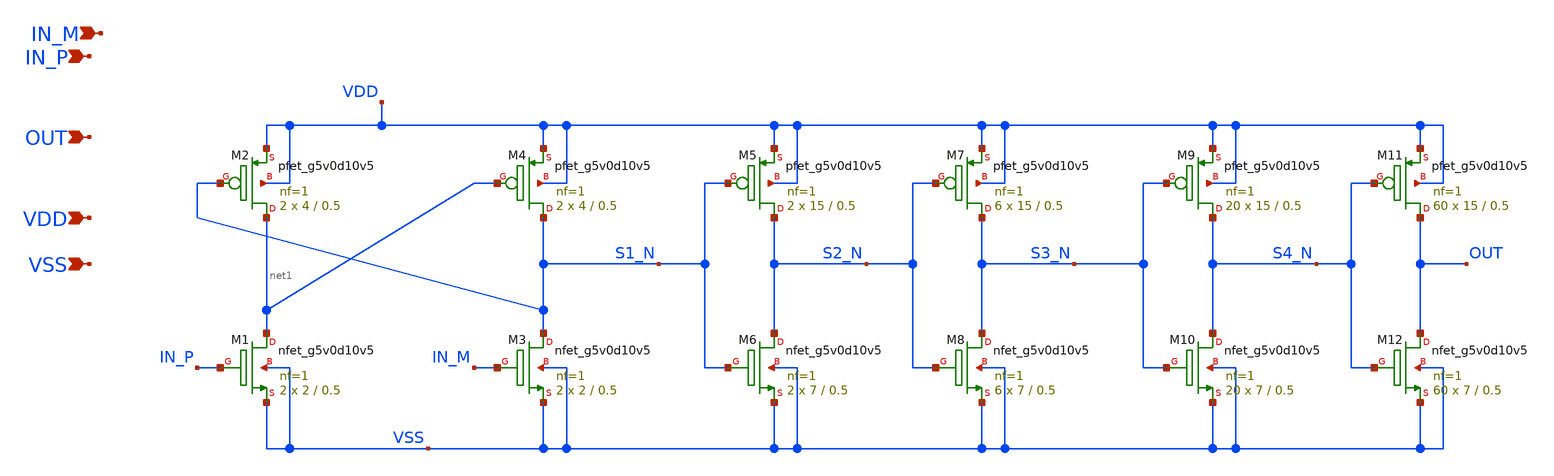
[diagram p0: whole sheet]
** sch_path: images/iic-osic-tools/addons/examples/open-pmic/design/power-stage/gate_drive.sch
**.subckt gate_drive IN_M IN_P OUT VDD VSS
*.ipin IN_M
*.ipin IN_P
*.ipin OUT
*.ipin VDD
*.ipin VSS
XM1 net1 IN_P VSS VSS sky130_fd_pr__nfet_g5v0d10v5 L=0.5 W=2 nf=1 ad='int((nf+1)/2) * W/nf * 0.29' as='int((nf+2)/2) * W/nf * 0.29'
+ pd='2*int((nf+1)/2) * (W/nf + 0.29)' ps='2*int((nf+2)/2) * (W/nf + 0.29)' nrd='0.29 / W' nrs='0.29 / W'
+ sa=0 sb=0 sd=0 mult=2 m=2
XM2 net1 S1_N VDD VDD sky130_fd_pr__pfet_g5v0d10v5 L=0.5 W=4 nf=1 ad='int((nf+1)/2) * W/nf * 0.29' as='int((nf+2)/2) * W/nf * 0.29'
+ pd='2*int((nf+1)/2) * (W/nf + 0.29)' ps='2*int((nf+2)/2) * (W/nf + 0.29)' nrd='0.29 / W' nrs='0.29 / W'
+ sa=0 sb=0 sd=0 mult=2 m=2
XM3 S1_N IN_M VSS VSS sky130_fd_pr__nfet_g5v0d10v5 L=0.5 W=2 nf=1 ad='int((nf+1)/2) * W/nf * 0.29' as='int((nf+2)/2) * W/nf * 0.29'
+ pd='2*int((nf+1)/2) * (W/nf + 0.29)' ps='2*int((nf+2)/2) * (W/nf + 0.29)' nrd='0.29 / W' nrs='0.29 / W'
+ sa=0 sb=0 sd=0 mult=2 m=2
XM4 S1_N net1 VDD VDD sky130_fd_pr__pfet_g5v0d10v5 L=0.5 W=4 nf=1 ad='int((nf+1)/2) * W/nf * 0.29' as='int((nf+2)/2) * W/nf * 0.29'
+ pd='2*int((nf+1)/2) * (W/nf + 0.29)' ps='2*int((nf+2)/2) * (W/nf + 0.29)' nrd='0.29 / W' nrs='0.29 / W'
+ sa=0 sb=0 sd=0 mult=2 m=2
XM5 S2_N S1_N VDD VDD sky130_fd_pr__pfet_g5v0d10v5 L=0.5 W=15 nf=1 ad='int((nf+1)/2) * W/nf * 0.29' as='int((nf+2)/2) * W/nf * 0.29'
+ pd='2*int((nf+1)/2) * (W/nf + 0.29)' ps='2*int((nf+2)/2) * (W/nf + 0.29)' nrd='0.29 / W' nrs='0.29 / W'
+ sa=0 sb=0 sd=0 mult=2 m=2
XM6 S2_N S1_N VSS VSS sky130_fd_pr__nfet_g5v0d10v5 L=0.5 W=7 nf=1 ad='int((nf+1)/2) * W/nf * 0.29' as='int((nf+2)/2) * W/nf * 0.29'
+ pd='2*int((nf+1)/2) * (W/nf + 0.29)' ps='2*int((nf+2)/2) * (W/nf + 0.29)' nrd='0.29 / W' nrs='0.29 / W'
+ sa=0 sb=0 sd=0 mult=2 m=2
XM7 S3_N S2_N VDD VDD sky130_fd_pr__pfet_g5v0d10v5 L=0.5 W=15 nf=1 ad='int((nf+1)/2) * W/nf * 0.29' as='int((nf+2)/2) * W/nf * 0.29'
+ pd='2*int((nf+1)/2) * (W/nf + 0.29)' ps='2*int((nf+2)/2) * (W/nf + 0.29)' nrd='0.29 / W' nrs='0.29 / W'
+ sa=0 sb=0 sd=0 mult=6 m=6
XM8 S3_N S2_N VSS VSS sky130_fd_pr__nfet_g5v0d10v5 L=0.5 W=7 nf=1 ad='int((nf+1)/2) * W/nf * 0.29' as='int((nf+2)/2) * W/nf * 0.29'
+ pd='2*int((nf+1)/2) * (W/nf + 0.29)' ps='2*int((nf+2)/2) * (W/nf + 0.29)' nrd='0.29 / W' nrs='0.29 / W'
+ sa=0 sb=0 sd=0 mult=6 m=6
XM9 S4_N S3_N VDD VDD sky130_fd_pr__pfet_g5v0d10v5 L=0.5 W=15 nf=1 ad='int((nf+1)/2) * W/nf * 0.29' as='int((nf+2)/2) * W/nf * 0.29'
+ pd='2*int((nf+1)/2) * (W/nf + 0.29)' ps='2*int((nf+2)/2) * (W/nf + 0.29)' nrd='0.29 / W' nrs='0.29 / W'
+ sa=0 sb=0 sd=0 mult=20 m=20
XM10 S4_N S3_N VSS VSS sky130_fd_pr__nfet_g5v0d10v5 L=0.5 W=7 nf=1 ad='int((nf+1)/2) * W/nf * 0.29' as='int((nf+2)/2) * W/nf * 0.29'
+ pd='2*int((nf+1)/2) * (W/nf + 0.29)' ps='2*int((nf+2)/2) * (W/nf + 0.29)' nrd='0.29 / W' nrs='0.29 / W'
+ sa=0 sb=0 sd=0 mult=20 m=20
XM11 OUT S4_N VDD VDD sky130_fd_pr__pfet_g5v0d10v5 L=0.5 W=15 nf=1 ad='int((nf+1)/2) * W/nf * 0.29' as='int((nf+2)/2) * W/nf * 0.29'
+ pd='2*int((nf+1)/2) * (W/nf + 0.29)' ps='2*int((nf+2)/2) * (W/nf + 0.29)' nrd='0.29 / W' nrs='0.29 / W'
+ sa=0 sb=0 sd=0 mult=60 m=60
XM12 OUT S4_N VSS VSS sky130_fd_pr__nfet_g5v0d10v5 L=0.5 W=7 nf=1 ad='int((nf+1)/2) * W/nf * 0.29' as='int((nf+2)/2) * W/nf * 0.29'
+ pd='2*int((nf+1)/2) * (W/nf + 0.29)' ps='2*int((nf+2)/2) * (W/nf + 0.29)' nrd='0.29 / W' nrs='0.29 / W'
+ sa=0 sb=0 sd=0 mult=60 m=60
**.ends
.end
